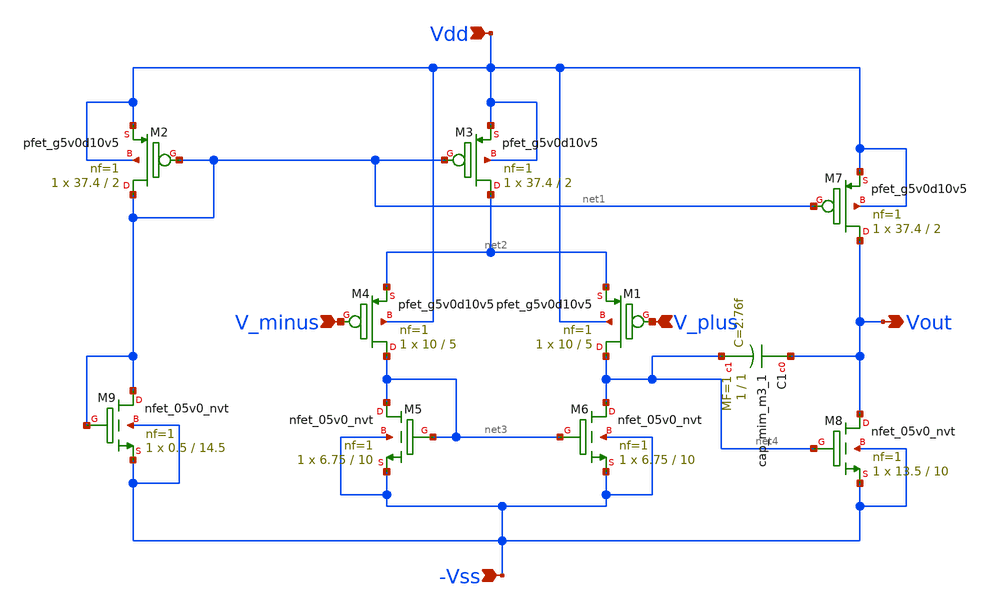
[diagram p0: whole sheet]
** sch_path: opamp_ckt.sch
**.subckt opamp_ckt Vdd V_minus V_plus -Vss Vout
*.ipin Vdd
*.ipin V_minus
*.ipin V_plus
*.ipin -Vss
*.opin Vout
XM2 net1 net1 Vdd Vdd sky130_fd_pr__pfet_g5v0d10v5 L=2 W=37.4 nf=1 ad='int((1 + 1)/2) * 37.4 / 1 * 0.29'
+ as='int((1 + 2)/2) * 37.4 / 1 * 0.29' pd='2*int((1 + 1)/2) * (37.4 / 1 + 0.29)' ps='2*int((1 + 2)/2) * (37.4 / 1 + 0.29)'
+ nrd='0.29 / 37.4 ' nrs='0.29 / 37.4 ' sa=0 sb=0 sd=0 mult=1 m=1
XM3 net2 net1 Vdd Vdd sky130_fd_pr__pfet_g5v0d10v5 L=2 W=37.4 nf=1 ad='int((1 + 1)/2) * 37.4 / 1 * 0.29'
+ as='int((1 + 2)/2) * 37.4 / 1 * 0.29' pd='2*int((1 + 1)/2) * (37.4 / 1 + 0.29)' ps='2*int((1 + 2)/2) * (37.4 / 1 + 0.29)'
+ nrd='0.29 / 37.4 ' nrs='0.29 / 37.4 ' sa=0 sb=0 sd=0 mult=1 m=1
XM5 net3 net3 -Vss -Vss sky130_fd_pr__nfet_05v0_nvt L=10 W=6.75 nf=1 ad='int((1 + 1)/2) * 6.75 / 1 * 0.29'
+ as='int((1 + 2)/2) * 6.75 / 1 * 0.29' pd='2*int((1 + 1)/2) * (6.75 / 1 + 0.29)' ps='2*int((1 + 2)/2) * (6.75 / 1 + 0.29)'
+ nrd='0.29 / 6.75 ' nrs='0.29 / 6.75 ' sa=0 sb=0 sd=0 mult=1 m=1
XM6 net4 net3 -Vss -Vss sky130_fd_pr__nfet_05v0_nvt L=10 W=6.75 nf=1 ad='int((1 + 1)/2) * 6.75 / 1 * 0.29'
+ as='int((1 + 2)/2) * 6.75 / 1 * 0.29' pd='2*int((1 + 1)/2) * (6.75 / 1 + 0.29)' ps='2*int((1 + 2)/2) * (6.75 / 1 + 0.29)'
+ nrd='0.29 / 6.75 ' nrs='0.29 / 6.75 ' sa=0 sb=0 sd=0 mult=1 m=1
XM7 Vout net1 Vdd Vdd sky130_fd_pr__pfet_g5v0d10v5 L=2 W=37.4 nf=1 ad='int((1 + 1)/2) * 37.4 / 1 * 0.29'
+ as='int((1 + 2)/2) * 37.4 / 1 * 0.29' pd='2*int((1 + 1)/2) * (37.4 / 1 + 0.29)' ps='2*int((1 + 2)/2) * (37.4 / 1 + 0.29)'
+ nrd='0.29 / 37.4 ' nrs='0.29 / 37.4 ' sa=0 sb=0 sd=0 mult=1 m=1
XM8 Vout net4 -Vss -Vss sky130_fd_pr__nfet_05v0_nvt L=10 W=13.5 nf=1 ad='int((1 + 1)/2) * 13.5 / 1 * 0.29'
+ as='int((1 + 2)/2) * 13.5 / 1 * 0.29' pd='2*int((1 + 1)/2) * (13.5 / 1 + 0.29)' ps='2*int((1 + 2)/2) * (13.5 / 1 + 0.29)'
+ nrd='0.29 / 13.5 ' nrs='0.29 / 13.5 ' sa=0 sb=0 sd=0 mult=1 m=1
XC1 Vout net4 sky130_fd_pr__cap_mim_m3_1 W=1 L=1 MF=1 m=1
XM1 net4 V_plus net2 Vdd sky130_fd_pr__pfet_g5v0d10v5 L=5 W=10 nf=1 ad='int((1 + 1)/2) * 10 / 1 * 0.29'
+ as='int((1 + 2)/2) * 10 / 1 * 0.29' pd='2*int((1 + 1)/2) * (10 / 1 + 0.29)' ps='2*int((1 + 2)/2) * (10 / 1 + 0.29)'
+ nrd='0.29 / 10 ' nrs='0.29 / 10 ' sa=0 sb=0 sd=0 mult=1 m=1
XM4 net3 V_minus net2 Vdd sky130_fd_pr__pfet_g5v0d10v5 L=5 W=10 nf=1 ad='int((1 + 1)/2) * 10 / 1 * 0.29'
+ as='int((1 + 2)/2) * 10 / 1 * 0.29' pd='2*int((1 + 1)/2) * (10 / 1 + 0.29)' ps='2*int((1 + 2)/2) * (10 / 1 + 0.29)'
+ nrd='0.29 / 10 ' nrs='0.29 / 10 ' sa=0 sb=0 sd=0 mult=1 m=1
XM9 net1 net1 -Vss -Vss sky130_fd_pr__nfet_05v0_nvt L=14.5 W=0.5 nf=1 ad='int((1 + 1)/2) * 0.5 / 1 * 0.29'
+ as='int((1 + 2)/2) * 0.5 / 1 * 0.29' pd='2*int((1 + 1)/2) * (0.5 / 1 + 0.29)' ps='2*int((1 + 2)/2) * (0.5 / 1 + 0.29)'
+ nrd='0.29 / 0.5 ' nrs='0.29 / 0.5 ' sa=0 sb=0 sd=0 mult=1 m=1
**.ends
.end
